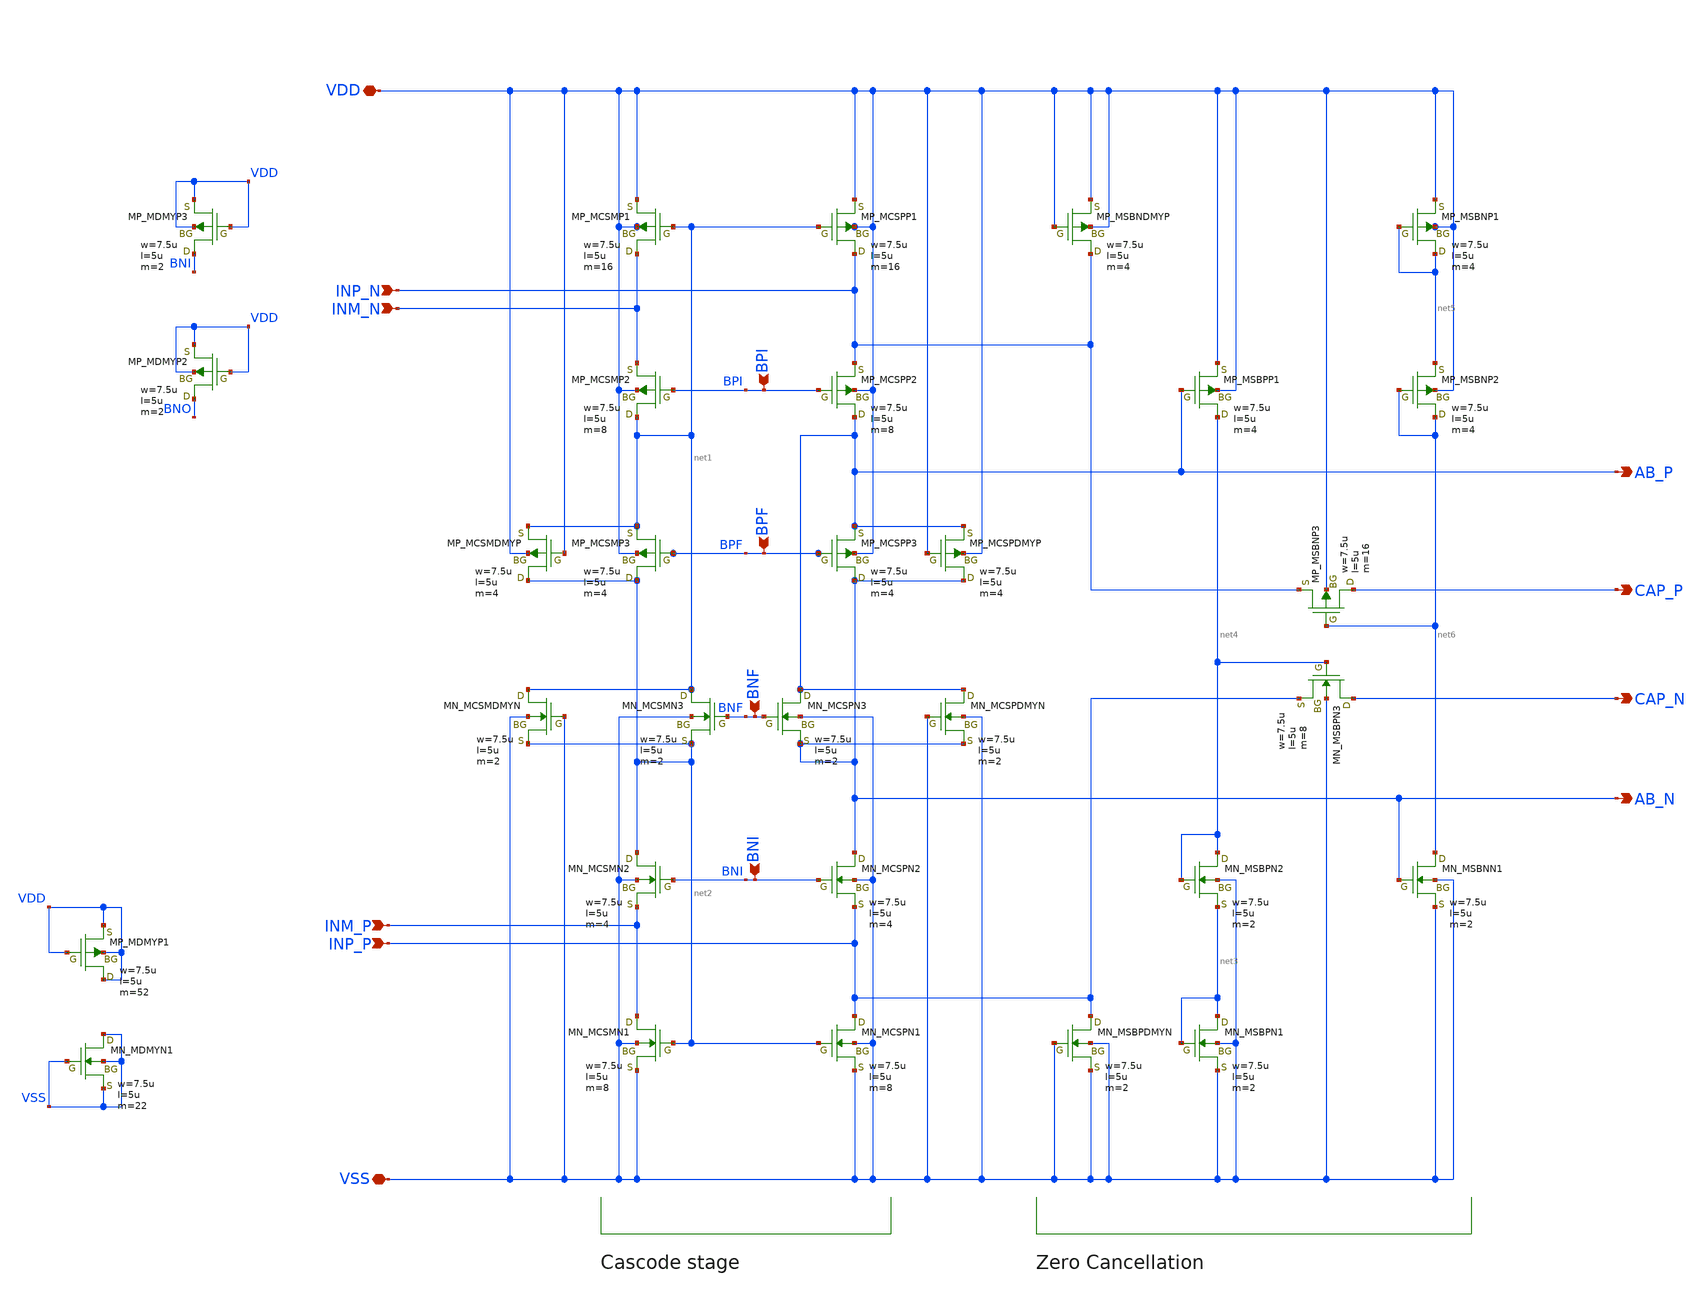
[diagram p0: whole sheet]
** sch_path: OpenSUSI-TR10/opamp_r2r_audio/opamp_r2r_cascode.sch
**.subckt opamp_r2r_cascode VDD VSS INP_N AB_P AB_N CAP_P CAP_N INM_N INM_P INP_P BPI BPF BNF BNI
*.iopin VDD
*.iopin VSS
*.ipin INP_N
*.opin AB_P
*.opin AB_N
*.opin CAP_P
*.opin CAP_N
*.ipin INM_N
*.ipin INM_P
*.ipin INP_P
*.ipin BPI
*.ipin BPF
*.ipin BNF
*.ipin BNI
XMCSMP1 INM_N net1 VDD VDD PMOS w=7.5u l=5u as=0 ad=0 ps=0 pd=0 nrd=0 nrs=0 m=16
XMCSMP2 net1 BPI INM_N VDD PMOS w=7.5u l=5u as=0 ad=0 ps=0 pd=0 nrd=0 nrs=0 m=8
XMCSMP3 net2 BPF net1 VDD PMOS w=7.5u l=5u as=0 ad=0 ps=0 pd=0 nrd=0 nrs=0 m=4
XMCSPP1 INP_N net1 VDD VDD PMOS w=7.5u l=5u as=0 ad=0 ps=0 pd=0 nrd=0 nrs=0 m=16
XMCSPP2 AB_P BPI INP_N VDD PMOS w=7.5u l=5u as=0 ad=0 ps=0 pd=0 nrd=0 nrs=0 m=8
XMCSPP3 AB_N BPF AB_P VDD PMOS w=7.5u l=5u as=0 ad=0 ps=0 pd=0 nrd=0 nrs=0 m=4
XMCSMN2 net2 BNI INM_P VSS NMOS w=7.5u l=5u as=0 ad=0 ps=0 pd=0 nrd=0 nrs=0 m=4
XMCSMN1 INM_P net2 VSS VSS NMOS w=7.5u l=5u as=0 ad=0 ps=0 pd=0 nrd=0 nrs=0 m=8
XMCSMN3 net1 BNF net2 VSS NMOS w=7.5u l=5u as=0 ad=0 ps=0 pd=0 nrd=0 nrs=0 m=2
XMCSPN3 AB_P BNF AB_N VSS NMOS w=7.5u l=5u as=0 ad=0 ps=0 pd=0 nrd=0 nrs=0 m=2
XMCSPN2 AB_N BNI INP_P VSS NMOS w=7.5u l=5u as=0 ad=0 ps=0 pd=0 nrd=0 nrs=0 m=4
XMCSPN1 INP_P net2 VSS VSS NMOS w=7.5u l=5u as=0 ad=0 ps=0 pd=0 nrd=0 nrs=0 m=8
XMSBPN2 net4 net4 net3 VSS NMOS w=7.5u l=5u as=0 ad=0 ps=0 pd=0 nrd=0 nrs=0 m=2
XMSBPN1 net3 net3 VSS VSS NMOS w=7.5u l=5u as=0 ad=0 ps=0 pd=0 nrd=0 nrs=0 m=2
XMSBPP1 net4 AB_P VDD VDD PMOS w=7.5u l=5u as=0 ad=0 ps=0 pd=0 nrd=0 nrs=0 m=4
XMSBNP1 net5 net5 VDD VDD PMOS w=7.5u l=5u as=0 ad=0 ps=0 pd=0 nrd=0 nrs=0 m=4
XMSBNP2 net6 net6 net5 VDD PMOS w=7.5u l=5u as=0 ad=0 ps=0 pd=0 nrd=0 nrs=0 m=4
XMSBNN1 net6 AB_N VSS VSS NMOS w=7.5u l=5u as=0 ad=0 ps=0 pd=0 nrd=0 nrs=0 m=2
XMSBNP3 CAP_P net6 INP_N VDD PMOS w=7.5u l=5u as=0 ad=0 ps=0 pd=0 nrd=0 nrs=0 m=16
XMSBPN3 CAP_N net4 INP_P VSS NMOS w=7.5u l=5u as=0 ad=0 ps=0 pd=0 nrd=0 nrs=0 m=8
XMSBPDMYN INP_P VSS VSS VSS NMOS w=7.5u l=5u as=0 ad=0 ps=0 pd=0 nrd=0 nrs=0 m=2
XMSBNDMYP INP_N VDD VDD VDD PMOS w=7.5u l=5u as=0 ad=0 ps=0 pd=0 nrd=0 nrs=0 m=4
XMDMYN1 VSS VSS VSS VSS NMOS w=7.5u l=5u as=0 ad=0 ps=0 pd=0 nrd=0 nrs=0 m=22
XMDMYP1 VDD VDD VDD VDD PMOS w=7.5u l=5u as=0 ad=0 ps=0 pd=0 nrd=0 nrs=0 m=52
XMDMYP2 BNO VDD VDD VDD PMOS w=7.5u l=5u as=0 ad=0 ps=0 pd=0 nrd=0 nrs=0 m=2
XMDMYP3 BNI VDD VDD VDD PMOS w=7.5u l=5u as=0 ad=0 ps=0 pd=0 nrd=0 nrs=0 m=2
XMCSMDMYP net2 VDD net1 VDD PMOS w=7.5u l=5u as=0 ad=0 ps=0 pd=0 nrd=0 nrs=0 m=4
XMCSPDMYP AB_N VDD AB_P VDD PMOS w=7.5u l=5u as=0 ad=0 ps=0 pd=0 nrd=0 nrs=0 m=4
XMCSMDMYN net1 VSS net2 VSS NMOS w=7.5u l=5u as=0 ad=0 ps=0 pd=0 nrd=0 nrs=0 m=2
XMCSPDMYN AB_P VSS AB_N VSS NMOS w=7.5u l=5u as=0 ad=0 ps=0 pd=0 nrd=0 nrs=0 m=2
**.ends
.end
